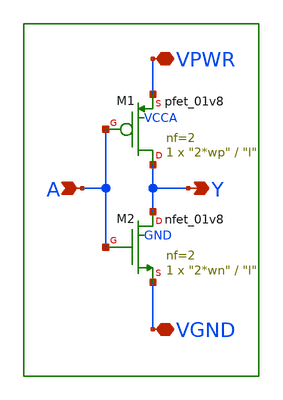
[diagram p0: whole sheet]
** sch_path: xschem/lib/main_inv_test.sch
**.subckt main_inv_test VPWR VGND A Y
*.iopin VPWR
*.iopin VGND
*.ipin A
*.opin Y
XM1 Y A VPWR VCCA sky130_fd_pr__pfet_01v8 L="l" W="2*wp" nf=2 ad='int((2 + 1)/2) * "2*wp" / 2 * 0.29'
+ as='int((2 + 2)/2) * "2*wp" / 2 * 0.29' pd='2*int((2 + 1)/2) * ("2*wp" / 2 + 0.29)' ps='2*int((2 + 2)/2) * ("2*wp" / 2 + 0.29)'
+ nrd='0.29 / "2*wp" ' nrs='0.29 / "2*wp" ' sa=0 sb=0 sd=0 mult=1 m=1
XM2 Y A VGND GND sky130_fd_pr__nfet_01v8 L="l" W="2*wn" nf=2 ad='int((nf+1)/2) * W/nf * 0.29' as='int((nf+2)/2) * W/nf * 0.29'
+ pd='2*int((nf+1)/2) * (W/nf + 0.29)' ps='2*int((nf+2)/2) * (W/nf + 0.29)' nrd='0.29 / W' nrs='0.29 / W'
+ sa=0 sb=0 sd=0 mult=1 m=1
**.ends
.end
